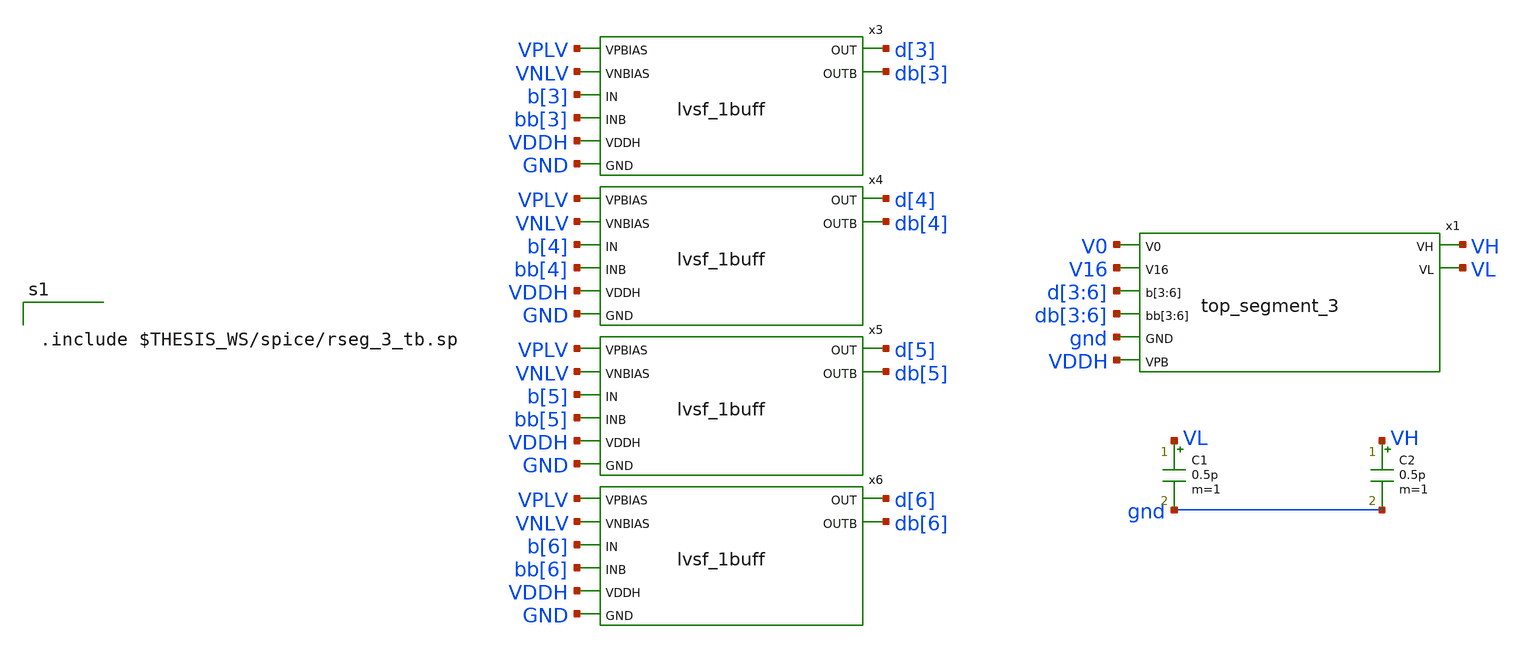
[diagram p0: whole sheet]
** sch_path: xschem/res_seg_3-tb.sch
.lib $::SKYWATER_MODELS/sky130.lib.spice tt
.include $::SKYWATER_STDCELLS/sky130_fd_sc_hd.spice
.include ~/pdk/sky130A/libs.ref/sky130_fd_sc_hvl/spice/sky130_fd_sc_hvl.spice

**.subckt res_seg_3-tb
x3 VPLV VNLV b[3] bb[3] d[3] db[3] VDDH GND lvsf_1buff
x4 VPLV VNLV b[4] bb[4] d[4] db[4] VDDH GND lvsf_1buff
x5 VPLV VNLV b[5] bb[5] d[5] db[5] VDDH GND lvsf_1buff
x6 VPLV VNLV b[6] bb[6] d[6] db[6] VDDH GND lvsf_1buff
C1 VL gnd 0.5p m=1
C2 VH gnd 0.5p m=1
x1 V0 V16 d[3] d[4] d[5] d[6] db[3] db[4] db[5] db[6] VH VL gnd VDDH top_segment_3
**** begin user architecture code


.include $THESIS_WS/spice/rseg_3_tb.sp

**** end user architecture code
**.ends

* expanding   symbol:  lvsf_1buff.sym # of pins=8
** sym_path: xschem/lvsf_1buff.sym
** sch_path: xschem/lvsf_1buff.sch
.subckt lvsf_1buff VPBIAS VNBIAS IN INB OUT OUTB VDDH GND
*.ipin IN
*.ipin INB
*.opin OUT
*.ipin VDDH
*.ipin GND
*.ipin VPBIAS
*.ipin VNBIAS
*.opin OUTB
XM13 n1 IN GND GND sky130_fd_pr__nfet_01v8 L=0.15 W=3 nf=1 ad='int((nf+1)/2) * W/nf * 0.29' as='int((nf+2)/2) * W/nf * 0.29'
+ pd='2*int((nf+1)/2) * (W/nf + 0.29)' ps='2*int((nf+2)/2) * (W/nf + 0.29)' nrd='0.29 / W' nrs='0.29 / W'
+ sa=0 sb=0 sd=0 mult=1 m=1
XM1 net2 VPBIAS VDDH VDDH sky130_fd_pr__pfet_g5v0d10v5 L=0.8 W=1 nf=1 ad='int((nf+1)/2) * W/nf * 0.29'
+ as='int((nf+2)/2) * W/nf * 0.29' pd='2*int((nf+1)/2) * (W/nf + 0.29)' ps='2*int((nf+2)/2) * (W/nf + 0.29)'
+ nrd='0.29 / W' nrs='0.29 / W' sa=0 sb=0 sd=0 mult=1 m=1
XM2 net1 VPBIAS VDDH VDDH sky130_fd_pr__pfet_g5v0d10v5 L=0.8 W=1 nf=1 ad='int((nf+1)/2) * W/nf * 0.29'
+ as='int((nf+2)/2) * W/nf * 0.29' pd='2*int((nf+1)/2) * (W/nf + 0.29)' ps='2*int((nf+2)/2) * (W/nf + 0.29)'
+ nrd='0.29 / W' nrs='0.29 / W' sa=0 sb=0 sd=0 mult=1 m=1
XM3 OUTPB OUTP net2 VDDH sky130_fd_pr__pfet_g5v0d10v5 L=0.8 W=1 nf=1 ad='int((nf+1)/2) * W/nf * 0.29'
+ as='int((nf+2)/2) * W/nf * 0.29' pd='2*int((nf+1)/2) * (W/nf + 0.29)' ps='2*int((nf+2)/2) * (W/nf + 0.29)'
+ nrd='0.29 / W' nrs='0.29 / W' sa=0 sb=0 sd=0 mult=1 m=1
XM4 OUTP OUTPB net1 VDDH sky130_fd_pr__pfet_g5v0d10v5 L=0.8 W=1 nf=1 ad='int((nf+1)/2) * W/nf * 0.29'
+ as='int((nf+2)/2) * W/nf * 0.29' pd='2*int((nf+1)/2) * (W/nf + 0.29)' ps='2*int((nf+2)/2) * (W/nf + 0.29)'
+ nrd='0.29 / W' nrs='0.29 / W' sa=0 sb=0 sd=0 mult=1 m=1
XM5 OUTPB VNBIAS n1 GND sky130_fd_pr__nfet_g5v0d10v5 L=1 W=1 nf=1 ad='int((nf+1)/2) * W/nf * 0.29' as='int((nf+2)/2) * W/nf * 0.29'
+ pd='2*int((nf+1)/2) * (W/nf + 0.29)' ps='2*int((nf+2)/2) * (W/nf + 0.29)' nrd='0.29 / W' nrs='0.29 / W'
+ sa=0 sb=0 sd=0 mult=1 m=1
XM6 OUTP VNBIAS n2 GND sky130_fd_pr__nfet_g5v0d10v5 L=1 W=1 nf=1 ad='int((nf+1)/2) * W/nf * 0.29' as='int((nf+2)/2) * W/nf * 0.29'
+ pd='2*int((nf+1)/2) * (W/nf + 0.29)' ps='2*int((nf+2)/2) * (W/nf + 0.29)' nrd='0.29 / W' nrs='0.29 / W'
+ sa=0 sb=0 sd=0 mult=1 m=1
XM7 n2 INB GND GND sky130_fd_pr__nfet_01v8 L=0.15 W=3 nf=1 ad='int((nf+1)/2) * W/nf * 0.29' as='int((nf+2)/2) * W/nf * 0.29'
+ pd='2*int((nf+1)/2) * (W/nf + 0.29)' ps='2*int((nf+2)/2) * (W/nf + 0.29)' nrd='0.29 / W' nrs='0.29 / W'
+ sa=0 sb=0 sd=0 mult=1 m=1
x1 OUTP GND GND VDDH VDDH OUTB sky130_fd_sc_hvl__inv_1
x2 OUTB GND GND VDDH VDDH OUT sky130_fd_sc_hvl__inv_1
.ends


* expanding   symbol:  top_segment_3.sym # of pins=8
** sym_path: xschem/top_segment_3.sym
** sch_path: xschem/top_segment_3.sch
.subckt top_segment_3 V0 V16 b[3] b[4] b[5] b[6] bb[3] bb[4] bb[5] bb[6] VH VL GND VPB
*.opin VH
*.ipin VPB
*.ipin b[3],b[4],b[5],b[6]
*.opin VL
*.ipin bb[3],bb[4],bb[5],bb[6]
*.ipin V16
*.ipin V0
*.ipin GND
x1 V0 V1 V2 V3 V4 V5 V6 V7 V8 bb[6] v1[0] v1[1] v1[2] v1[3] v1[4] v1[5] v1[6] v1[7] v1[8] VPB
+ switch_pmos_1g_9o
x2 V8 V9 V10 V11 V12 V13 V14 V15 V16 b[6] v1[0] v1[1] v1[2] v1[3] v1[4] v1[5] v1[6] v1[7] v1[8] VPB
+ switch_pmos_1g_9o
x3 v1[0] v1[1] v1[2] v1[3] v1[4] b[5] v2[0] v2[1] v2[2] v2[3] v2[4] VPB switch_pmos_1g_5o
x4 v1[4] v1[5] v1[6] v1[7] v1[8] bb[5] v2[0] v2[1] v2[2] v2[3] v2[4] VPB switch_pmos_1g_5o
x5 v2[0] v2[1] v2[2] b[4] v3[0] v3[1] v3[2] VPB switch_pmos_1g_3o
x6 v2[2] v2[3] v2[4] bb[4] v3[0] v3[1] v3[2] VPB switch_pmos_1g_3o
x7 v3[0] v3[1] b[3] VH VL VPB switch_pmos_1g_2o
x8 v3[1] v3[2] bb[3] VH VL VPB switch_pmos_1g_2o
x9 V0 V1 V2 V3 V4 V5 V6 V7 V8 V9 V10 V11 V12 V13 V14 V15 V16 GND rseg_3_v3
.ends


* expanding   symbol:  switch_pmos_1g_9o.sym # of pins=4
** sym_path: xschem/switch_pmos_1g_9o.sym
** sch_path: xschem/switch_pmos_1g_9o.sch
.subckt switch_pmos_1g_9o vin[0] vin[1] vin[2] vin[3] vin[4] vin[5] vin[6] vin[7] vin[8] DIN vout[0]
+ vout[1] vout[2] vout[3] vout[4] vout[5] vout[6] vout[7] vout[8] VPB
*.ipin vin[0],vin[1],vin[2],vin[3],vin[4],vin[5],vin[6],vin[7],vin[8]
*.opin vout[0],vout[1],vout[2],vout[3],vout[4],vout[5],vout[6],vout[7],vout[8]
*.ipin VPB
*.ipin DIN
.param wp=0.42 wn=0.42 l=0.5

XM1 vout[0] DIN vin[0] VPB sky130_fd_pr__pfet_g5v0d10v5 L=l W=wp nf=1 ad='int((nf+1)/2) * W/nf * 0.29'
+ as='int((nf+2)/2) * W/nf * 0.29' pd='2*int((nf+1)/2) * (W/nf + 0.29)' ps='2*int((nf+2)/2) * (W/nf + 0.29)'
+ nrd='0.29 / W' nrs='0.29 / W' sa=0 sb=0 sd=0 mult=1 m=1
XM2 vout[1] DIN vin[1] VPB sky130_fd_pr__pfet_g5v0d10v5 L=l W=wp nf=1 ad='int((nf+1)/2) * W/nf * 0.29'
+ as='int((nf+2)/2) * W/nf * 0.29' pd='2*int((nf+1)/2) * (W/nf + 0.29)' ps='2*int((nf+2)/2) * (W/nf + 0.29)'
+ nrd='0.29 / W' nrs='0.29 / W' sa=0 sb=0 sd=0 mult=1 m=1
XM3 vout[2] DIN vin[2] VPB sky130_fd_pr__pfet_g5v0d10v5 L=l W=wp nf=1 ad='int((nf+1)/2) * W/nf * 0.29'
+ as='int((nf+2)/2) * W/nf * 0.29' pd='2*int((nf+1)/2) * (W/nf + 0.29)' ps='2*int((nf+2)/2) * (W/nf + 0.29)'
+ nrd='0.29 / W' nrs='0.29 / W' sa=0 sb=0 sd=0 mult=1 m=1
XM4 vout[3] DIN vin[3] VPB sky130_fd_pr__pfet_g5v0d10v5 L=l W=wp nf=1 ad='int((nf+1)/2) * W/nf * 0.29'
+ as='int((nf+2)/2) * W/nf * 0.29' pd='2*int((nf+1)/2) * (W/nf + 0.29)' ps='2*int((nf+2)/2) * (W/nf + 0.29)'
+ nrd='0.29 / W' nrs='0.29 / W' sa=0 sb=0 sd=0 mult=1 m=1
XM5 vout[4] DIN vin[4] VPB sky130_fd_pr__pfet_g5v0d10v5 L=l W=wp nf=1 ad='int((nf+1)/2) * W/nf * 0.29'
+ as='int((nf+2)/2) * W/nf * 0.29' pd='2*int((nf+1)/2) * (W/nf + 0.29)' ps='2*int((nf+2)/2) * (W/nf + 0.29)'
+ nrd='0.29 / W' nrs='0.29 / W' sa=0 sb=0 sd=0 mult=1 m=1
XM6 vout[5] DIN vin[5] VPB sky130_fd_pr__pfet_g5v0d10v5 L=l W=wp nf=1 ad='int((nf+1)/2) * W/nf * 0.29'
+ as='int((nf+2)/2) * W/nf * 0.29' pd='2*int((nf+1)/2) * (W/nf + 0.29)' ps='2*int((nf+2)/2) * (W/nf + 0.29)'
+ nrd='0.29 / W' nrs='0.29 / W' sa=0 sb=0 sd=0 mult=1 m=1
XM7 vout[6] DIN vin[6] VPB sky130_fd_pr__pfet_g5v0d10v5 L=l W=wp nf=1 ad='int((nf+1)/2) * W/nf * 0.29'
+ as='int((nf+2)/2) * W/nf * 0.29' pd='2*int((nf+1)/2) * (W/nf + 0.29)' ps='2*int((nf+2)/2) * (W/nf + 0.29)'
+ nrd='0.29 / W' nrs='0.29 / W' sa=0 sb=0 sd=0 mult=1 m=1
XM8 vout[7] DIN vin[7] VPB sky130_fd_pr__pfet_g5v0d10v5 L=l W=wp nf=1 ad='int((nf+1)/2) * W/nf * 0.29'
+ as='int((nf+2)/2) * W/nf * 0.29' pd='2*int((nf+1)/2) * (W/nf + 0.29)' ps='2*int((nf+2)/2) * (W/nf + 0.29)'
+ nrd='0.29 / W' nrs='0.29 / W' sa=0 sb=0 sd=0 mult=1 m=1
XM9 vout[8] DIN vin[8] VPB sky130_fd_pr__pfet_g5v0d10v5 L=l W=wp nf=1 ad='int((nf+1)/2) * W/nf * 0.29'
+ as='int((nf+2)/2) * W/nf * 0.29' pd='2*int((nf+1)/2) * (W/nf + 0.29)' ps='2*int((nf+2)/2) * (W/nf + 0.29)'
+ nrd='0.29 / W' nrs='0.29 / W' sa=0 sb=0 sd=0 mult=1 m=1
.ends


* expanding   symbol:  switch_pmos_1g_5o.sym # of pins=4
** sym_path: xschem/switch_pmos_1g_5o.sym
** sch_path: xschem/switch_pmos_1g_5o.sch
.subckt switch_pmos_1g_5o vin[0] vin[1] vin[2] vin[3] vin[4] DIN vout[0] vout[1] vout[2] vout[3]
+ vout[4] VPB
*.ipin vin[0],vin[1],vin[2],vin[3],vin[4]
*.opin vout[0],vout[1],vout[2],vout[3],vout[4]
*.ipin VPB
*.ipin DIN
.param wp=0.42 wn=0.42 l=0.5

XM1 vout[0] DIN vin[0] VPB sky130_fd_pr__pfet_g5v0d10v5 L=l W=wp nf=1 ad='int((nf+1)/2) * W/nf * 0.29'
+ as='int((nf+2)/2) * W/nf * 0.29' pd='2*int((nf+1)/2) * (W/nf + 0.29)' ps='2*int((nf+2)/2) * (W/nf + 0.29)'
+ nrd='0.29 / W' nrs='0.29 / W' sa=0 sb=0 sd=0 mult=1 m=1
XM2 vout[1] DIN vin[1] VPB sky130_fd_pr__pfet_g5v0d10v5 L=l W=wp nf=1 ad='int((nf+1)/2) * W/nf * 0.29'
+ as='int((nf+2)/2) * W/nf * 0.29' pd='2*int((nf+1)/2) * (W/nf + 0.29)' ps='2*int((nf+2)/2) * (W/nf + 0.29)'
+ nrd='0.29 / W' nrs='0.29 / W' sa=0 sb=0 sd=0 mult=1 m=1
XM3 vout[2] DIN vin[2] VPB sky130_fd_pr__pfet_g5v0d10v5 L=l W=wp nf=1 ad='int((nf+1)/2) * W/nf * 0.29'
+ as='int((nf+2)/2) * W/nf * 0.29' pd='2*int((nf+1)/2) * (W/nf + 0.29)' ps='2*int((nf+2)/2) * (W/nf + 0.29)'
+ nrd='0.29 / W' nrs='0.29 / W' sa=0 sb=0 sd=0 mult=1 m=1
XM4 vout[3] DIN vin[3] VPB sky130_fd_pr__pfet_g5v0d10v5 L=l W=wp nf=1 ad='int((nf+1)/2) * W/nf * 0.29'
+ as='int((nf+2)/2) * W/nf * 0.29' pd='2*int((nf+1)/2) * (W/nf + 0.29)' ps='2*int((nf+2)/2) * (W/nf + 0.29)'
+ nrd='0.29 / W' nrs='0.29 / W' sa=0 sb=0 sd=0 mult=1 m=1
XM5 vout[4] DIN vin[4] VPB sky130_fd_pr__pfet_g5v0d10v5 L=l W=wp nf=1 ad='int((nf+1)/2) * W/nf * 0.29'
+ as='int((nf+2)/2) * W/nf * 0.29' pd='2*int((nf+1)/2) * (W/nf + 0.29)' ps='2*int((nf+2)/2) * (W/nf + 0.29)'
+ nrd='0.29 / W' nrs='0.29 / W' sa=0 sb=0 sd=0 mult=1 m=1
.ends


* expanding   symbol:  switch_pmos_1g_3o.sym # of pins=4
** sym_path: xschem/switch_pmos_1g_3o.sym
** sch_path: xschem/switch_pmos_1g_3o.sch
.subckt switch_pmos_1g_3o vin[0] vin[1] vin[2] DIN vout[0] vout[1] vout[2] VPB
*.ipin vin[0],vin[1],vin[2]
*.opin vout[0],vout[1],vout[2]
*.ipin VPB
*.ipin DIN
.param wp=0.42 wn=0.42 l=0.5

XM1 vout[0] DIN vin[0] VPB sky130_fd_pr__pfet_g5v0d10v5 L=l W=wp nf=1 ad='int((nf+1)/2) * W/nf * 0.29'
+ as='int((nf+2)/2) * W/nf * 0.29' pd='2*int((nf+1)/2) * (W/nf + 0.29)' ps='2*int((nf+2)/2) * (W/nf + 0.29)'
+ nrd='0.29 / W' nrs='0.29 / W' sa=0 sb=0 sd=0 mult=1 m=1
XM2 vout[1] DIN vin[1] VPB sky130_fd_pr__pfet_g5v0d10v5 L=l W=wp nf=1 ad='int((nf+1)/2) * W/nf * 0.29'
+ as='int((nf+2)/2) * W/nf * 0.29' pd='2*int((nf+1)/2) * (W/nf + 0.29)' ps='2*int((nf+2)/2) * (W/nf + 0.29)'
+ nrd='0.29 / W' nrs='0.29 / W' sa=0 sb=0 sd=0 mult=1 m=1
XM3 vout[2] DIN vin[2] VPB sky130_fd_pr__pfet_g5v0d10v5 L=l W=wp nf=1 ad='int((nf+1)/2) * W/nf * 0.29'
+ as='int((nf+2)/2) * W/nf * 0.29' pd='2*int((nf+1)/2) * (W/nf + 0.29)' ps='2*int((nf+2)/2) * (W/nf + 0.29)'
+ nrd='0.29 / W' nrs='0.29 / W' sa=0 sb=0 sd=0 mult=1 m=1
.ends


* expanding   symbol:  switch_pmos_1g_2o.sym # of pins=5
** sym_path: xschem/switch_pmos_1g_2o.sym
** sch_path: xschem/switch_pmos_1g_2o.sch
.subckt switch_pmos_1g_2o vin[0] vin[1] DIN VH VL VPB
*.ipin vin[0],vin[1]
*.opin VH
*.ipin VPB
*.ipin DIN
*.opin VL
.param wp=0.42 wn=0.42 l=0.5

XM1 VL DIN vin[0] VPB sky130_fd_pr__pfet_g5v0d10v5 L=l W=wp nf=1 ad='int((nf+1)/2) * W/nf * 0.29' as='int((nf+2)/2) * W/nf * 0.29'
+ pd='2*int((nf+1)/2) * (W/nf + 0.29)' ps='2*int((nf+2)/2) * (W/nf + 0.29)' nrd='0.29 / W' nrs='0.29 / W'
+ sa=0 sb=0 sd=0 mult=1 m=1
XM2 VH DIN vin[1] VPB sky130_fd_pr__pfet_g5v0d10v5 L=l W=wp nf=1 ad='int((nf+1)/2) * W/nf * 0.29' as='int((nf+2)/2) * W/nf * 0.29'
+ pd='2*int((nf+1)/2) * (W/nf + 0.29)' ps='2*int((nf+2)/2) * (W/nf + 0.29)' nrd='0.29 / W' nrs='0.29 / W'
+ sa=0 sb=0 sd=0 mult=1 m=1
.ends

.end
